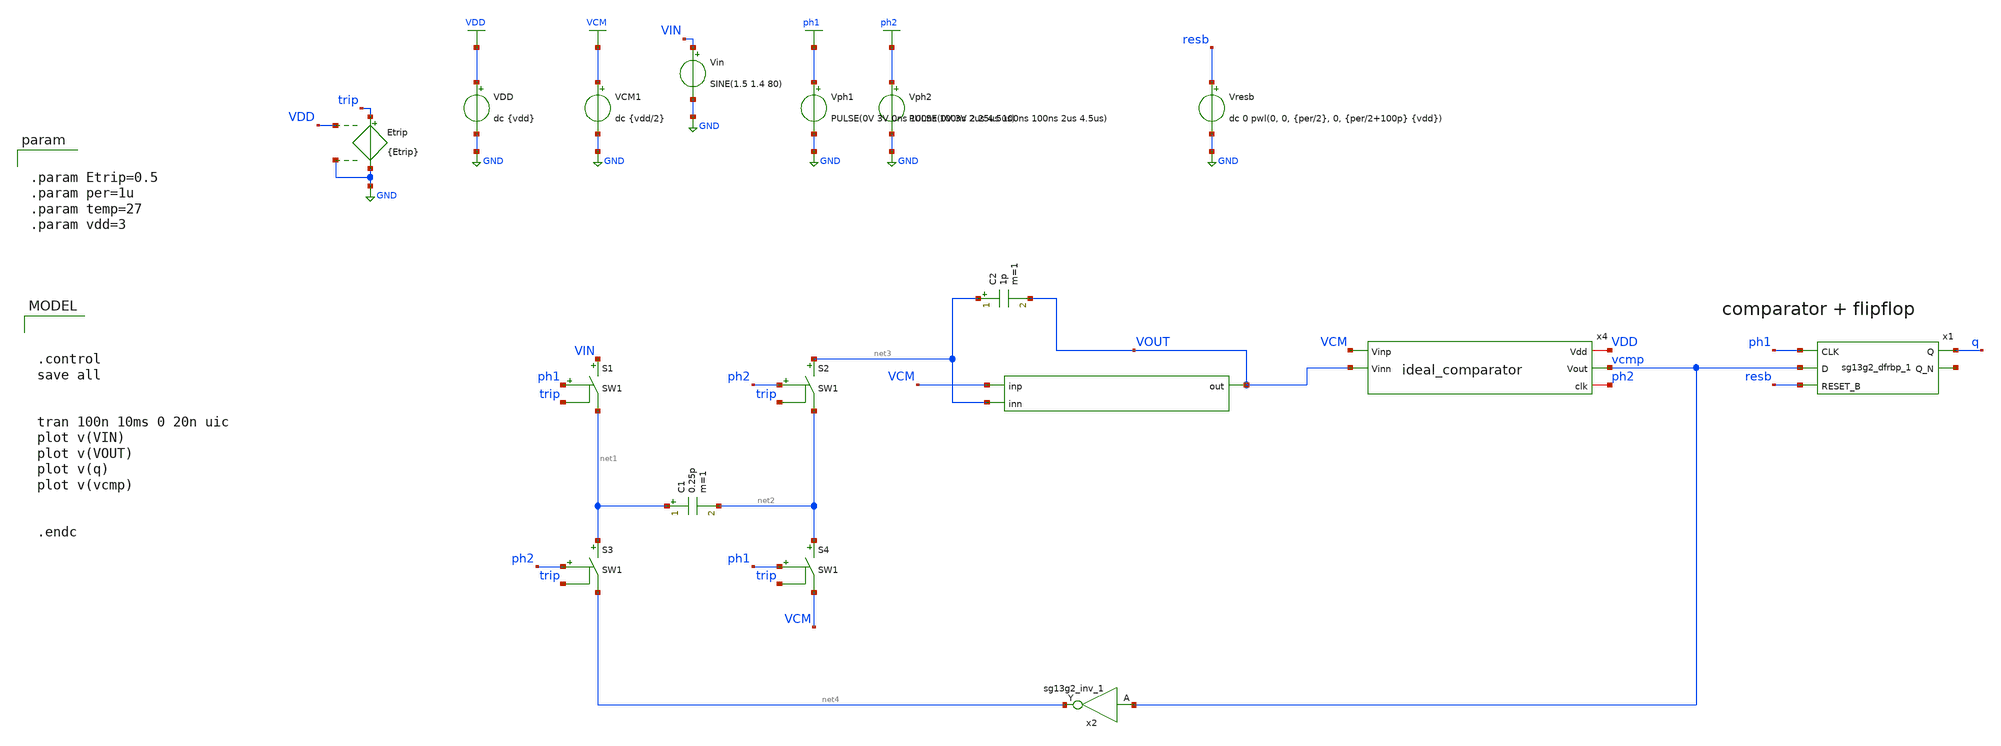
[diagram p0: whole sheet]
** sch_path: DSM_1storder/Schematic_Level/xschem/ideal_DSM_1order.sch
**.subckt ideal_DSM_1order
C1 net1 net2 0.25p m=1
S2 net3 net2 ph2 trip SW1
S3 net1 net4 ph2 trip SW1
S4 net2 VCM ph1 trip SW1
VDD VDD GND dc {vdd}
VCM1 VCM GND dc {vdd/2}
Vph2 ph2 GND PULSE(0V 3V 2.25us 100ns 100ns 2us 4.5us)
Vph1 ph1 GND PULSE(0V 3V 0ns 100ns 100ns 2us 4.5us)
C2 net3 VOUT 1p m=1
x1 q net5 ph1 vcmp resb VDD VSS sg13g2_dfrbp_1
Vresb resb GND dc 0 pwl(0, 0, {per/2}, 0, {per/2+100p} {vdd})
x2 net4 vcmp 3 0 sg13g2_inv_1
S1 VIN net1 ph1 trip SW1
Etrip trip GND VDD GND {Etrip}
Vin VIN GND SINE(1.5 1.4 80)
x3 VOUT VCM net3 ideal_opamp
x4 VDD vcmp VCM ph2 VOUT ideal_comparator
**** begin user architecture code



.control
save all


tran 100n 10ms 0 20n uic
plot v(VIN)
plot v(VOUT)
plot v(q)
plot v(vcmp)


.endc



.lib $::SG13G2_MODELS/cornerMOSlv.lib mos_tt
.lib $::SG13G2_MODELS/cornerRES.lib res_typ
.inc /foss/pdks/ihp-sg13g2/libs.ref/sg13g2_stdcell/spice/sg13g2_stdcell.spice



.param Etrip=0.5
.param per=1u
.param temp=27
.param vdd=3


**** end user architecture code
**.ends
.GLOBAL GND
.GLOBAL VDD
.GLOBAL VCM
.GLOBAL ph2
.GLOBAL ph1
**** begin user architecture code
.MODEL SW1 SW(VT=0.5 VH=0 RON=0.1 ROFF=100M)
**** end user architecture code
.end
